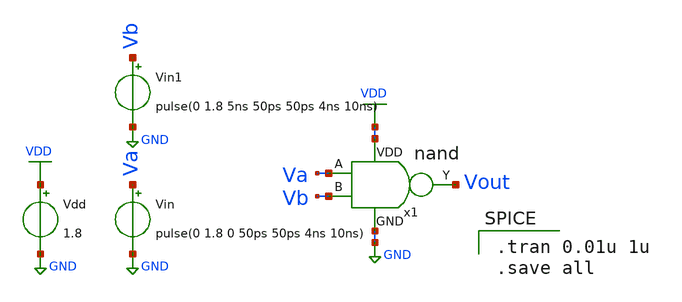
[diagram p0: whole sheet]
** sch_path: designs/nand/xschem/nand_tb.sch
**.subckt nand_tb
Vdd VDD GND 1.8
Vin Va GND pulse(0 1.8 0 50ps 50ps 4ns 10ns)
x1 VDD Va Vb Vout GND nand
Vin1 Vb GND pulse(0 1.8 5ns 50ps 50ps 4ns 10ns)
**** begin user architecture code

** opencircuidesign pdks install
.lib /home/ubvm/Desktop/chip_design/open_pdks/sky130/sky130A/libs.tech/ngspice/sky130.lib.spice tt_mm




.tran 0.01u 1u
.save all

**** end user architecture code
**.ends

* expanding   symbol:  /home/ubvm/unic-cass/nand/nand.sym # of pins=5
** sym_path: designs/nand/xschem/nand.sym
** sch_path: designs/nand/xschem/nand.sch
.subckt nand VDD A B Y GND
*.ipin A
*.ipin B
*.opin Y
*.iopin GND
*.iopin VDD
XM1 Y B GND GND sky130_fd_pr__nfet_01v8 L=0.15 W=1 nf=1 ad='int((1 + 1)/2) * 1 / 1 * 0.29' as='int((1 + 2)/2) * 1 / 1 * 0.29'
+ pd='2*int((1 + 1)/2) * (1 / 1 + 0.29)' ps='2*int((1 + 2)/2) * (1 / 1 + 0.29)' nrd='0.29 / 1 ' nrs='0.29 / 1 '
+ sa=0 sb=0 sd=0 mult=1 m=1
XM2 Y A net1 net1 sky130_fd_pr__pfet_01v8 L=0.15 W=1 nf=1 ad='int((1 + 1)/2) * 1 / 1 * 0.29' as='int((1 + 2)/2) * 1 / 1 * 0.29'
+ pd='2*int((1 + 1)/2) * (1 / 1 + 0.29)' ps='2*int((1 + 2)/2) * (1 / 1 + 0.29)' nrd='0.29 / 1 ' nrs='0.29 / 1 '
+ sa=0 sb=0 sd=0 mult=1 m=1
XM3 net1 B VDD VDD sky130_fd_pr__pfet_01v8 L=0.15 W=1 nf=1 ad='int((1 + 1)/2) * 1 / 1 * 0.29' as='int((1 + 2)/2) * 1 / 1 * 0.29'
+ pd='2*int((1 + 1)/2) * (1 / 1 + 0.29)' ps='2*int((1 + 2)/2) * (1 / 1 + 0.29)' nrd='0.29 / 1 ' nrs='0.29 / 1 '
+ sa=0 sb=0 sd=0 mult=1 m=1
XM4 Y A GND GND sky130_fd_pr__nfet_01v8 L=0.15 W=1 nf=1 ad='int((1 + 1)/2) * 1 / 1 * 0.29' as='int((1 + 2)/2) * 1 / 1 * 0.29'
+ pd='2*int((1 + 1)/2) * (1 / 1 + 0.29)' ps='2*int((1 + 2)/2) * (1 / 1 + 0.29)' nrd='0.29 / 1 ' nrs='0.29 / 1 '
+ sa=0 sb=0 sd=0 mult=1 m=1
.ends

.GLOBAL VDD
.GLOBAL GND
.end
